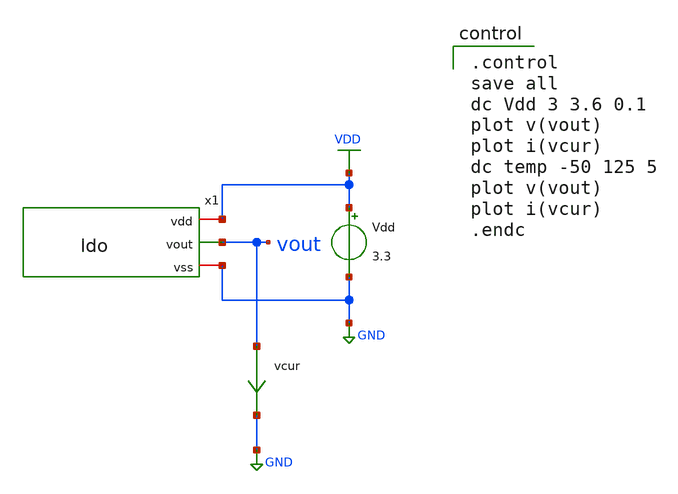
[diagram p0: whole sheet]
** sch_path: noritsuna/ldo/ldo_tb.sch
**.subckt ldo_tb
Vdd VDD GND 3.3
x1 VDD vout GND ldo
vcur vout GND 0
.save i(vcur)
**** begin user architecture code

.control
save all
dc Vdd 3 3.6 0.1
plot v(vout)
plot i(vcur)
dc temp -50 125 5
plot v(vout)
plot i(vcur)
.endc


.include $::180MCU_MODELS/design.ngspice
.lib $::180MCU_MODELS/sm141064.ngspice typical
.lib $::180MCU_MODELS/sm141064.ngspice res_typical
.lib $::180MCU_MODELS/sm141064.ngspice cap_mim
.lib $::180MCU_MODELS/sm141064.ngspice moscap_typical
.lib $::180MCU_MODELS/sm141064.ngspice mimcap_typical
.lib $::180MCU_MODELS/sm141064.ngspice bjt_typical
* .lib $::180MCU_MODELS/sm141064.ngspice res_statistical

**** end user architecture code
**.ends
.GLOBAL VDD
.GLOBAL GND
.end
